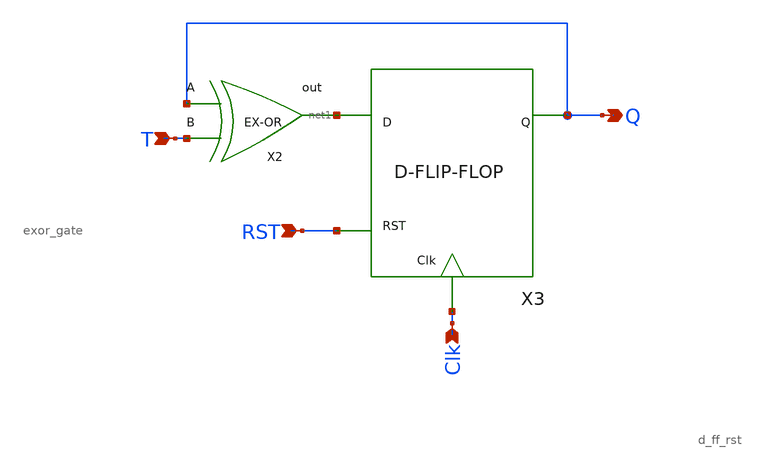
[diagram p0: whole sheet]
** sch_path: xschem/T_flip_flop/t_ff_rst.sch
**.subckt t_ff_rst T Clk Q RST
*.ipin T
*.ipin Clk
*.opin Q
*.ipin RST
X2 Q T net1 exor_gate
X3 net1 Q Clk RST d_ff_rst
**.ends

* expanding   symbol:  exor_gate/exor_gate.sym # of pins=3
** sym_path: xschem/exor_gate/exor_gate.sym
** sch_path: xschem/exor_gate/exor_gate.sch
.subckt exor_gate A B out
*.ipin A
*.ipin B
*.opin out
XM4 out A net1 GND sky130_fd_pr__nfet_01v8 L=0.18 W=0.5 nf=1 ad='int((nf+1)/2) * W/nf * 0.29' as='int((nf+2)/2) * W/nf * 0.29'
+ pd='2*int((nf+1)/2) * (W/nf + 0.29)' ps='2*int((nf+2)/2) * (W/nf + 0.29)' nrd='0.29 / W' nrs='0.29 / W'
+ sa=0 sb=0 sd=0 mult=1 m=1
XM5 net3 B VDD VDD sky130_fd_pr__pfet_01v8 L=0.18 W=1 nf=1 ad='int((nf+1)/2) * W/nf * 0.29' as='int((nf+2)/2) * W/nf * 0.29'
+ pd='2*int((nf+1)/2) * (W/nf + 0.29)' ps='2*int((nf+2)/2) * (W/nf + 0.29)' nrd='0.29 / W' nrs='0.29 / W'
+ sa=0 sb=0 sd=0 mult=1 m=1
XM1 net1 B GND GND sky130_fd_pr__nfet_01v8 L=0.18 W=0.5 nf=1 ad='int((nf+1)/2) * W/nf * 0.29' as='int((nf+2)/2) * W/nf * 0.29'
+ pd='2*int((nf+1)/2) * (W/nf + 0.29)' ps='2*int((nf+2)/2) * (W/nf + 0.29)' nrd='0.29 / W' nrs='0.29 / W'
+ sa=0 sb=0 sd=0 mult=1 m=1
XM2 out net5 net3 VDD sky130_fd_pr__pfet_01v8 L=0.18 W=1 nf=1 ad='int((nf+1)/2) * W/nf * 0.29' as='int((nf+2)/2) * W/nf * 0.29'
+ pd='2*int((nf+1)/2) * (W/nf + 0.29)' ps='2*int((nf+2)/2) * (W/nf + 0.29)' nrd='0.29 / W' nrs='0.29 / W'
+ sa=0 sb=0 sd=0 mult=1 m=1
XM3 net4 net6 VDD VDD sky130_fd_pr__pfet_01v8 L=0.18 W=1 nf=1 ad='int((nf+1)/2) * W/nf * 0.29' as='int((nf+2)/2) * W/nf * 0.29'
+ pd='2*int((nf+1)/2) * (W/nf + 0.29)' ps='2*int((nf+2)/2) * (W/nf + 0.29)' nrd='0.29 / W' nrs='0.29 / W'
+ sa=0 sb=0 sd=0 mult=1 m=1
XM6 out A net4 VDD sky130_fd_pr__pfet_01v8 L=0.18 W=1 nf=1 ad='int((nf+1)/2) * W/nf * 0.29' as='int((nf+2)/2) * W/nf * 0.29'
+ pd='2*int((nf+1)/2) * (W/nf + 0.29)' ps='2*int((nf+2)/2) * (W/nf + 0.29)' nrd='0.29 / W' nrs='0.29 / W'
+ sa=0 sb=0 sd=0 mult=1 m=1
XM7 out net5 net2 GND sky130_fd_pr__nfet_01v8 L=0.18 W=0.5 nf=1 ad='int((nf+1)/2) * W/nf * 0.29' as='int((nf+2)/2) * W/nf * 0.29'
+ pd='2*int((nf+1)/2) * (W/nf + 0.29)' ps='2*int((nf+2)/2) * (W/nf + 0.29)' nrd='0.29 / W' nrs='0.29 / W'
+ sa=0 sb=0 sd=0 mult=1 m=1
XM8 net2 net6 GND GND sky130_fd_pr__nfet_01v8 L=0.18 W=0.5 nf=1 ad='int((nf+1)/2) * W/nf * 0.29' as='int((nf+2)/2) * W/nf * 0.29'
+ pd='2*int((nf+1)/2) * (W/nf + 0.29)' ps='2*int((nf+2)/2) * (W/nf + 0.29)' nrd='0.29 / W' nrs='0.29 / W'
+ sa=0 sb=0 sd=0 mult=1 m=1
X3 B net6 inv Wpmos=3 Lpmos=0.18 Wnmos=1 Lnmos=0.18
X2 A net5 inv Wpmos=3 Lpmos=0.18 Wnmos=1 Lnmos=0.18
.ends


* expanding   symbol:  D_flip_flop/d_ff_rst.sym # of pins=4
** sym_path: xschem/D_flip_flop/d_ff_rst.sym
** sch_path: xschem/D_flip_flop/d_ff_rst.sch
.subckt d_ff_rst D Q Clk RST
*.ipin D
*.ipin Clk
*.opin Q
*.ipin RST
X1 net1 net2 inv Wpmos=3 Lpmos=0.18 Wnmos=1 Lnmos=0.18
X2 net3 Q inv Wpmos=3 Lpmos=0.18 Wnmos=1 Lnmos=0.18
X3 net2 net4 inv Wpmos=3 Lpmos=0.18 Wnmos=1 Lnmos=0.18
X4 Q net5 inv Wpmos=3 Lpmos=0.18 Wnmos=1 Lnmos=0.18
X5 net7 net1 Clk net6 transmission_gate Wpmos=1 Lpmos=0.18 Wnmos=1 Lnmos=0.18
X6 net1 net4 net6 Clk transmission_gate Wpmos=1 Lpmos=0.18 Wnmos=1 Lnmos=0.18
X7 net3 net5 Clk net6 transmission_gate Wpmos=1 Lpmos=0.18 Wnmos=1 Lnmos=0.18
X8 net2 net3 net6 Clk transmission_gate Wpmos=1 Lpmos=0.18 Wnmos=1 Lnmos=0.18
X9 Clk net6 inv Wpmos=3 Lpmos=0.18 Wnmos=1 Lnmos=0.18
X10 net8 D net7 and_gate
X11 RST net8 inv Wpmos=3 Lpmos=0.18 Wnmos=1 Lnmos=0.18
.ends


* expanding   symbol:  inv/inv.sym # of pins=2
** sym_path: xschem/inv/inv.sym
** sch_path: xschem/inv/inv.sch
.subckt inv in out  Wpmos=3 Lpmos=0.18 Wnmos=1 Lnmos=0.18
*.ipin in
*.iopin out
XM1 out in GND GND sky130_fd_pr__nfet_01v8 L=Lnmos W=Wnmos nf=1 ad='int((nf+1)/2) * W/nf * 0.29' as='int((nf+2)/2) * W/nf * 0.29'
+ pd='2*int((nf+1)/2) * (W/nf + 0.29)' ps='2*int((nf+2)/2) * (W/nf + 0.29)' nrd='0.29 / W' nrs='0.29 / W'
+ sa=0 sb=0 sd=0 mult=1 m=1
XM2 out in VDD VDD sky130_fd_pr__pfet_01v8 L=Lpmos W=Wpmos nf=1 ad='int((nf+1)/2) * W/nf * 0.29' as='int((nf+2)/2) * W/nf * 0.29'
+ pd='2*int((nf+1)/2) * (W/nf + 0.29)' ps='2*int((nf+2)/2) * (W/nf + 0.29)' nrd='0.29 / W' nrs='0.29 / W'
+ sa=0 sb=0 sd=0 mult=1 m=1
.ends


* expanding   symbol:  transmission_gate/transmission_gate.sym # of pins=4
** sym_path: xschem/transmission_gate/transmission_gate.sym
** sch_path: xschem/transmission_gate/transmission_gate.sch
.subckt transmission_gate in out ctrl_ ctrl  Wpmos=1 Lpmos=0.18 Wnmos=1 Lnmos=0.18
*.iopin in
*.iopin out
*.ipin ctrl_
*.ipin ctrl
XM1 in ctrl out GND sky130_fd_pr__nfet_01v8 L=Lnmos W=Wnmos nf=1 ad='int((nf+1)/2) * W/nf * 0.29' as='int((nf+2)/2) * W/nf * 0.29'
+ pd='2*int((nf+1)/2) * (W/nf + 0.29)' ps='2*int((nf+2)/2) * (W/nf + 0.29)' nrd='0.29 / W' nrs='0.29 / W'
+ sa=0 sb=0 sd=0 mult=1 m=1
XM2 out ctrl_ in VDD sky130_fd_pr__pfet_01v8 L=Lpmos W=Wpmos nf=1 ad='int((nf+1)/2) * W/nf * 0.29' as='int((nf+2)/2) * W/nf * 0.29'
+ pd='2*int((nf+1)/2) * (W/nf + 0.29)' ps='2*int((nf+2)/2) * (W/nf + 0.29)' nrd='0.29 / W' nrs='0.29 / W'
+ sa=0 sb=0 sd=0 mult=1 m=1
.ends


* expanding   symbol:  and_gate/and_gate.sym # of pins=3
** sym_path: xschem/and_gate/and_gate.sym
** sch_path: xschem/and_gate/and_gate.sch
.subckt and_gate A B out
*.ipin A
*.ipin B
*.opin out
XM1 net1 A net2 GND sky130_fd_pr__nfet_01v8 L=0.18 W=1 nf=1 ad='int((nf+1)/2) * W/nf * 0.29' as='int((nf+2)/2) * W/nf * 0.29'
+ pd='2*int((nf+1)/2) * (W/nf + 0.29)' ps='2*int((nf+2)/2) * (W/nf + 0.29)' nrd='0.29 / W' nrs='0.29 / W'
+ sa=0 sb=0 sd=0 mult=1 m=1
XM2 net1 A VDD VDD sky130_fd_pr__pfet_01v8 L=0.18 W=1 nf=1 ad='int((nf+1)/2) * W/nf * 0.29' as='int((nf+2)/2) * W/nf * 0.29'
+ pd='2*int((nf+1)/2) * (W/nf + 0.29)' ps='2*int((nf+2)/2) * (W/nf + 0.29)' nrd='0.29 / W' nrs='0.29 / W'
+ sa=0 sb=0 sd=0 mult=1 m=1
XM3 net1 B VDD VDD sky130_fd_pr__pfet_01v8 L=0.18 W=1 nf=1 ad='int((nf+1)/2) * W/nf * 0.29' as='int((nf+2)/2) * W/nf * 0.29'
+ pd='2*int((nf+1)/2) * (W/nf + 0.29)' ps='2*int((nf+2)/2) * (W/nf + 0.29)' nrd='0.29 / W' nrs='0.29 / W'
+ sa=0 sb=0 sd=0 mult=1 m=1
XM4 net2 B GND GND sky130_fd_pr__nfet_01v8 L=0.18 W=1 nf=1 ad='int((nf+1)/2) * W/nf * 0.29' as='int((nf+2)/2) * W/nf * 0.29'
+ pd='2*int((nf+1)/2) * (W/nf + 0.29)' ps='2*int((nf+2)/2) * (W/nf + 0.29)' nrd='0.29 / W' nrs='0.29 / W'
+ sa=0 sb=0 sd=0 mult=1 m=1
X1 net1 out inv Wpmos=3 Lpmos=0.18 Wnmos=1 Lnmos=0.18
.ends

.GLOBAL VDD
.GLOBAL GND
.end
